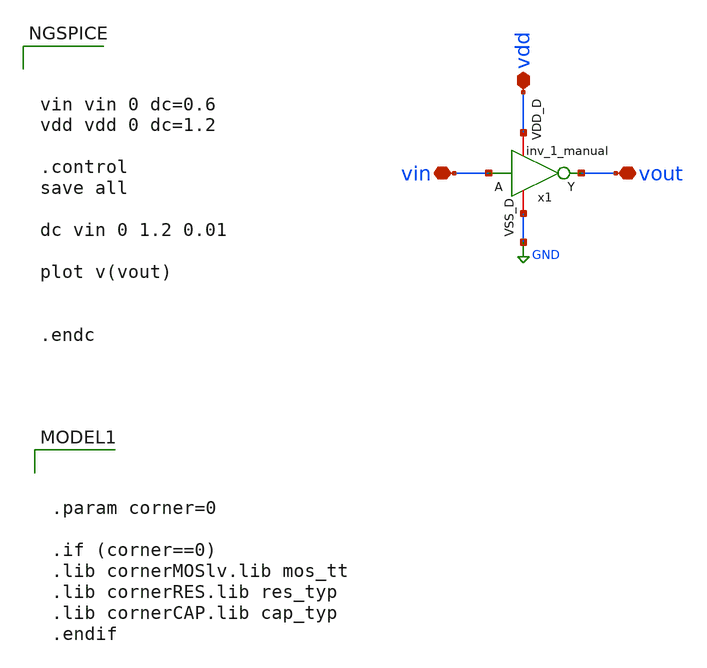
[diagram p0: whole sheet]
** sch_path: Day1/tb_inv_1_manual.sch
**.subckt tb_inv_1_manual vin vout vdd
*.iopin vin
*.iopin vout
*.iopin vdd
x1 vdd vin vout GND inv_1_manual
**** begin user architecture code



vin vin 0 dc=0.6
vdd vdd 0 dc=1.2

.control
save all

dc vin 0 1.2 0.01

plot v(vout)


.endc




.param corner=0

.if (corner==0)
.lib cornerMOSlv.lib mos_tt
.lib cornerRES.lib res_typ
.lib cornerCAP.lib cap_typ
.endif

**** end user architecture code
**.ends

* expanding   symbol:  inv_1_manual.sym # of pins=4
** sym_path: Day1/inv_1_manual.sym
** sch_path: Day1/inv_1_manual.sch
.subckt inv_1_manual VDD_D A Y VSS_D
*.iopin VDD_D
*.iopin VSS_D
*.iopin A
*.iopin Y
XM1 VSS_D A Y VSS_D sg13_lv_nmos w=0.74u l=0.13u ng=1 m=1 mm_ok=1
XM2 Y A VDD_D VDD_D sg13_lv_pmos w=1.12u l=0.13u ng=1 m=1 mm_ok=1
.ends

.GLOBAL GND
.end
